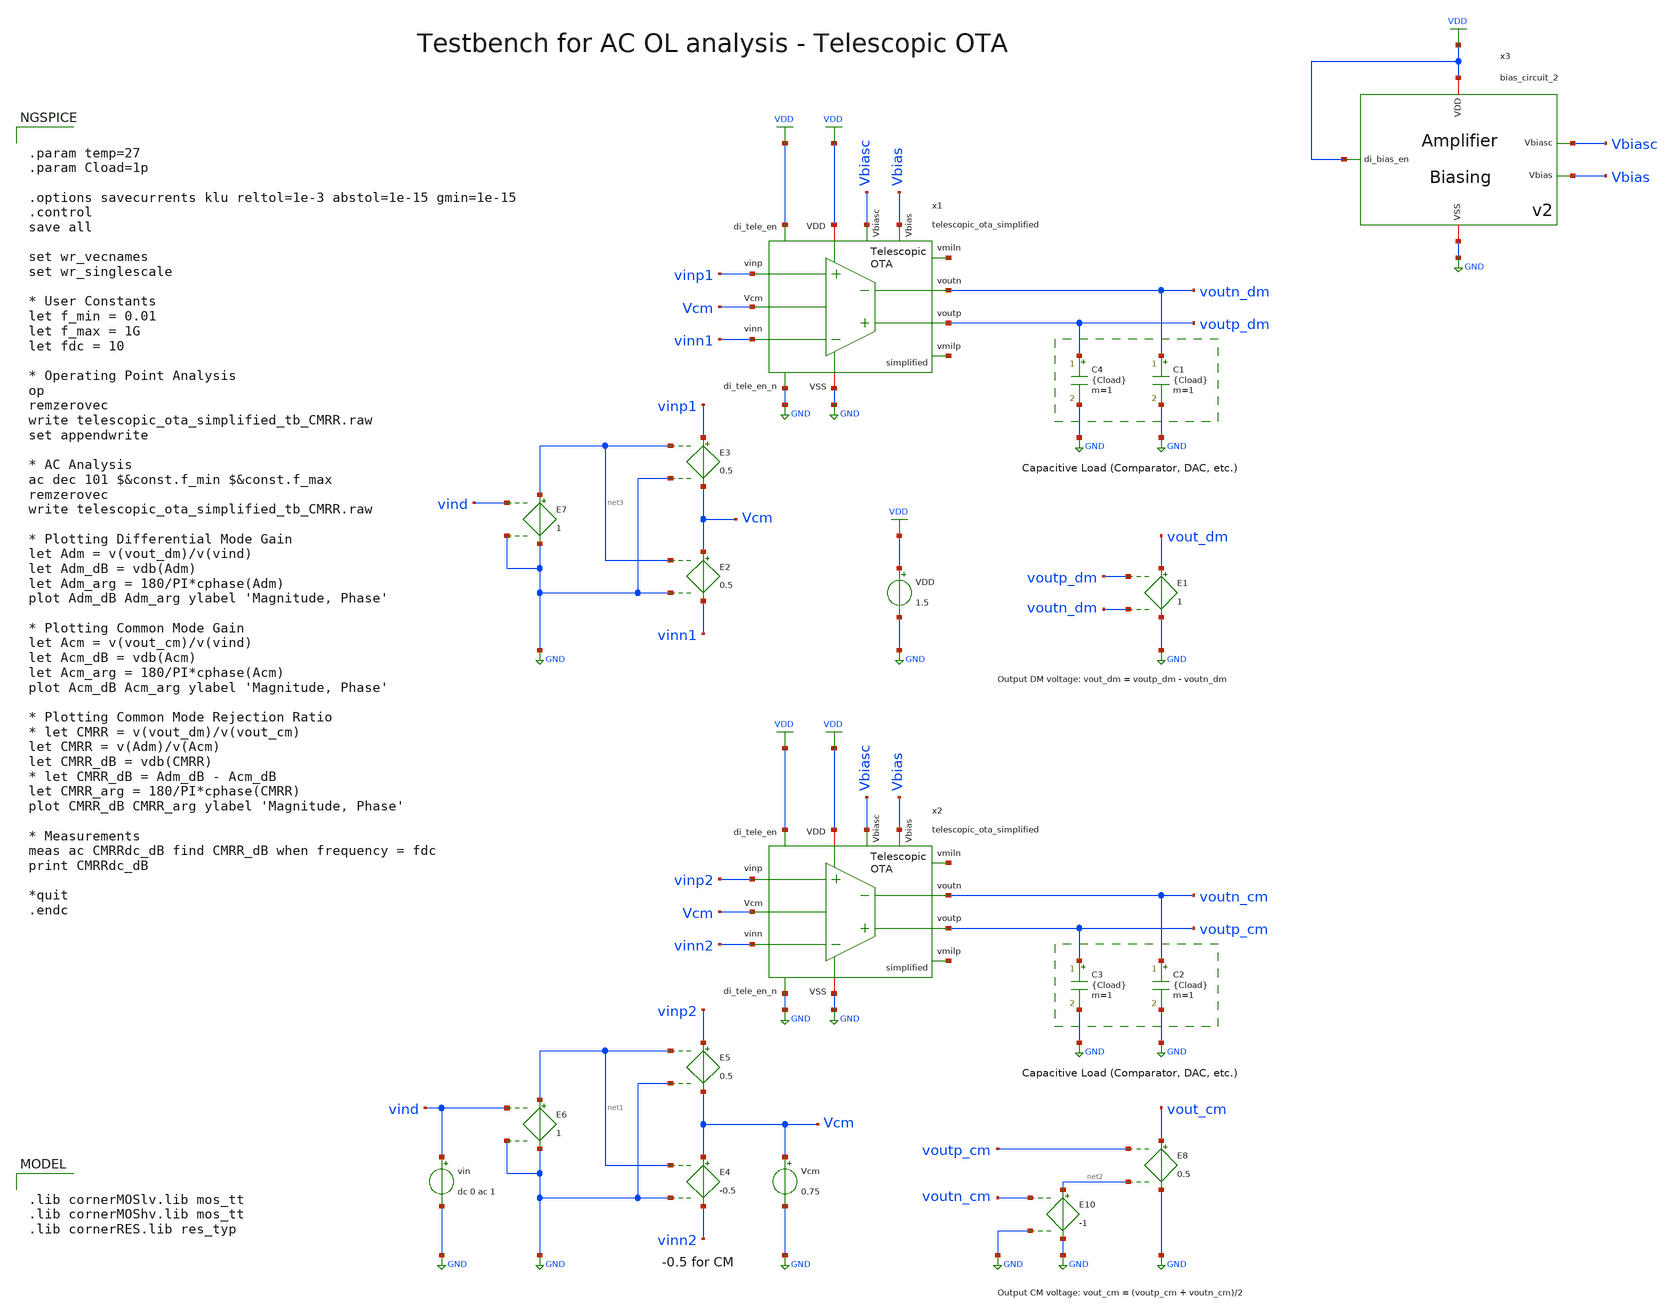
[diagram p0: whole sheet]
** sch_path: SG13G2_ATBS-ADC-main/xschem/bio_amplifier/amplifier_core/telescopic_ota/testbenches/telescopic_ota_simplified_tb_CMRR.sch
**.subckt telescopic_ota_simplified_tb_CMRR
VDD VDD GND 1.5
Vcm Vcm GND 0.75
E4 Vcm vinn2 net1 GND -0.5
E5 vinp2 Vcm net1 GND 0.5
E6 net1 GND vind GND 1
vin vind GND dc 0 ac 1
C2 voutn_cm GND {Cload} m=1
C3 voutp_cm GND {Cload} m=1
E1 vout_dm GND voutp_dm voutn_dm 1
E8 vout_cm GND voutp_cm net2 0.5
E10 net2 GND voutn_cm GND -1
E2 Vcm vinn1 net3 GND 0.5
E3 vinp1 Vcm net3 GND 0.5
E7 net3 GND vind GND 1
C1 voutn_dm GND {Cload} m=1
C4 voutp_dm GND {Cload} m=1
x1 net4 net5 voutp_dm voutn_dm VDD vinn1 vinp1 GND Vcm VDD GND Vbiasc Vbias
+ telescopic_ota_simplified
x2 net6 net7 voutp_cm voutn_cm VDD vinn2 vinp2 GND Vcm VDD GND Vbiasc Vbias
+ telescopic_ota_simplified
x3 VDD Vbiasc VDD GND Vbias bias_circuit_2
**** begin user architecture code


.param temp=27
.param Cload=1p

.options savecurrents klu reltol=1e-3 abstol=1e-15 gmin=1e-15
.control
save all

set wr_vecnames
set wr_singlescale

* User Constants
let f_min = 0.01
let f_max = 1G
let fdc = 10

* Operating Point Analysis
op
remzerovec
write telescopic_ota_simplified_tb_CMRR.raw
set appendwrite

* AC Analysis
ac dec 101 $&const.f_min $&const.f_max
remzerovec
write telescopic_ota_simplified_tb_CMRR.raw

* Plotting Differential Mode Gain
let Adm = v(vout_dm)/v(vind)
let Adm_dB = vdb(Adm)
let Adm_arg = 180/PI*cphase(Adm)
plot Adm_dB Adm_arg ylabel 'Magnitude, Phase'

* Plotting Common Mode Gain
let Acm = v(vout_cm)/v(vind)
let Acm_dB = vdb(Acm)
let Acm_arg = 180/PI*cphase(Acm)
plot Acm_dB Acm_arg ylabel 'Magnitude, Phase'

* Plotting Common Mode Rejection Ratio
* let CMRR = v(vout_dm)/v(vout_cm)
let CMRR = v(Adm)/v(Acm)
let CMRR_dB = vdb(CMRR)
* let CMRR_dB = Adm_dB - Acm_dB
let CMRR_arg = 180/PI*cphase(CMRR)
plot CMRR_dB CMRR_arg ylabel 'Magnitude, Phase'

* Measurements
meas ac CMRRdc_dB find CMRR_dB when frequency = fdc
print CMRRdc_dB

*quit
.endc



.lib cornerMOSlv.lib mos_tt
.lib cornerMOShv.lib mos_tt
.lib cornerRES.lib res_typ

**** end user architecture code
**.ends

* expanding   symbol:  bio_amplifier/amplifier_core/telescopic_ota/telescopic_ota_simplified.sym #
*+ of pins=13
** sym_path: SG13G2_ATBS-ADC-main/xschem/bio_amplifier/amplifier_core/telescopic_ota/telescopic_ota_simplified.sym
** sch_path: SG13G2_ATBS-ADC-main/xschem/bio_amplifier/amplifier_core/telescopic_ota/telescopic_ota_simplified.sch
.subckt telescopic_ota_simplified vmiln vmilp voutp voutn VDD vinn vinp VSS Vcm di_tele_en
+ di_tele_en_n Vbiasc Vbias
*.ipin vinp
*.ipin vinn
*.opin voutp
*.opin voutn
*.iopin VDD
*.iopin VSS
*.ipin Vcm
*.ipin di_tele_en
*.ipin di_tele_en_n
*.ipin vmilp
*.ipin vmiln
*.ipin Vbias
*.ipin Vbiasc
R1 net1 voutn 25.5Meg m=1
C1 net1 voutn 900f m=1
C2 voutp net1 900f m=1
R2 voutp net1 25.5Meg m=1
xM6 net3 Vgs_m56 VDD VDD sg13g2_lv_pmos_stacked_x2 W_P=1.0u L_P=20.0u NG_P=1 M_P=1
xM5 net2 Vgs_m56 VDD VDD sg13g2_lv_pmos_stacked_x2 W_P=8.0u L_P=20.0u NG_P=8 M_P=1
xM5c Vtail net10 net2 net2 sg13g2_lv_pmos_stacked_x2 W_P=8.0u L_P=20.0u NG_P=8 M_P=1
xM7 net7 net7 net6 net6 sg13g2_lv_pmos_stacked_x2 W_P=0.5u L_P=20.0u NG_P=1 M_P=1
XM1 vmiln vinp net4 net6 sg13_lv_pmos w=250.0u l=10.0u ng=250 m=1 mm_ok=1
XM1c voutn net7 vmiln vmiln sg13_lv_pmos w=15.0u l=10.0u ng=15 m=1 mm_ok=1
XM2c voutp net7 vmilp vmilp sg13_lv_pmos w=15.0u l=10.0u ng=15 m=1 mm_ok=1
XM2 vmilp vinn net5 net6 sg13_lv_pmos w=250.0u l=10.0u ng=250 m=1 mm_ok=1
xM3 voutn net1 VSS VSS sg13g2_lv_nmos_stacked_x4 W_N=1.5u L_N=40.0u NG_N=1 M_N=1
xM4 voutp net1 VSS VSS sg13g2_lv_nmos_stacked_x4 W_N=1.5u L_N=40.0u NG_N=1 M_N=1
Vmeas net9 net4 0
.save i(vmeas)
Vmeas1 net9 net5 0
.save i(vmeas1)
Vmeas2 net9 net6 0
.save i(vmeas2)
xM6c net8 net10 net3 net3 sg13g2_lv_pmos_stacked_x2 W_P=1.0u L_P=20.0u NG_P=1 M_P=1
XMpd4 Vcm di_tele_en_n net10 VDD sg13_hv_pmos w=1.0u l=0.5u ng=1 m=1 mm_ok=1
XMdec1 VDD Vgs_m56 VDD VDD sg13_lv_pmos w=10.0u l=40.0u ng=10 m=1 mm_ok=1
XMpd3 net10 di_tele_en VDD VDD sg13_hv_pmos w=1.0u l=0.5u ng=1 m=1 mm_ok=1
XMpd2 net8 di_tele_en_n Vgs_m56 VDD sg13_hv_pmos w=1.0u l=0.5u ng=1 m=1 mm_ok=1
XMpd1 Vgs_m56 di_tele_en VDD VDD sg13_hv_pmos w=1.0u l=0.5u ng=1 m=1 mm_ok=1
XMdec3 VDD net10 VDD VDD sg13_lv_pmos w=10.0u l=40.0u ng=10 m=1 mm_ok=1
Vmeas3 net8 net12 0
.save i(vmeas3)
Vmeas4 net7 net14 0
.save i(vmeas4)
xM8c net12 Vbiasc VSS net11 sg13g2_lv_nmos_stacked_x2 W_N=20.0u L_N=20.0u NG_N=20 M_N=1
xM8 net11 Vbias VSS VSS sg13g2_lv_nmos_stacked_x2 W_N=20.0u L_N=20.0u NG_N=20 M_N=1
xM9c net14 Vbiasc VSS net13 sg13g2_lv_nmos_stacked_x2 W_N=10.0u L_N=20.0u NG_N=10 M_N=1
xM9 net13 Vbias VSS VSS sg13g2_lv_nmos_stacked_x2 W_N=10.0u L_N=20.0u NG_N=10 M_N=1
Vmeas5 Vtail net9 0
.save i(vmeas5)
.ends


* expanding   symbol:  bio_amplifier/amplifier_core/bias_circuit/bias_circuit_2/bias_circuit_2.sym #
*+ of pins=5
** sym_path: SG13G2_ATBS-ADC-main/xschem/bio_amplifier/amplifier_core/bias_circuit/bias_circuit_2/bias_circuit_2.sym
** sch_path: SG13G2_ATBS-ADC-main/xschem/bio_amplifier/amplifier_core/bias_circuit/bias_circuit_2/bias_circuit_2.sch
.subckt bias_circuit_2 di_bias_en Vbiasc VDD VSS Vbias
*.iopin VDD
*.iopin VSS
*.opin Vbias
*.ipin di_bias_en
*.opin Vbiasc
R1 net3 VSS 3.72Meg m=1
XMDEC1 net1 Vbias net1 net1 sg13_lv_nmos w=100.0u l=40.0u ng=100 m=1 mm_ok=1
VIref net4 net8 0
.save i(viref)
VIout net9 Vbiasc 0
.save i(viout)
x1 VDD di_bias_en bias_en_n VSS inverter_lv W_P=1.0u L_P=0.13u W_N=1.0u L_N=0.13u
xMSU2 Vsu net6 VSS VSS sg13g2_lv_nmos_stacked_x4 W_N=1.0u L_N=40.0u NG_N=1 M_N=1
xMSU1 net5 Vsu VSS net6 sg13g2_lv_nmos_stacked_x4 W_N=1.0u L_N=40.0u NG_N=1 M_N=1
Vmeas1 net4 net5 0
.save i(vmeas1)
Vmeas2 Vbias net6 0
.save i(vmeas2)
XMPD1 Vgs_m34 di_bias_en net2 net2 sg13_lv_pmos w=1.0u l=0.13u ng=1 m=1 mm_ok=1
XMPD2 net4 bias_en_n Vgs_m34 net2 sg13_lv_pmos w=1.0u l=0.13u ng=1 m=1 mm_ok=1
XMPD3 Vbias bias_en_n VSS VSS sg13_lv_nmos w=1.0u l=0.13u ng=1 m=1 mm_ok=1
VIref5 net1 VSS 0
.save i(viref5)
VIdd VDD net2 0
.save i(vidd)
CSU1 net10 Vsu 35f m=1
xM1 net7 Vbias VSS net3 sg13g2_lv_nmos_stacked_x2 W_N=20.0u L_N=20.0u NG_N=20 M_N=1
xM1c net8 Vbiasc VSS net7 sg13g2_lv_nmos_stacked_x2 W_N=5.0u L_N=20.0u NG_N=5 M_N=1
xM2 Vbias Vbias VSS VSS sg13g2_lv_nmos_stacked_x2 W_N=5.0u L_N=20.0u NG_N=5 M_N=1
xM2c Vbiasc Vbiasc VSS Vbias sg13g2_lv_nmos_stacked_x2 W_N=5.0u L_N=20.0u NG_N=5 M_N=1
XMDEC2 net2 Vgs_m34 net2 net2 sg13_lv_pmos w=25.0u l=40.0u ng=25 m=1 mm_ok=1
xM3 net4 Vgs_m34 net2 net2 sg13g2_lv_pmos_stacked_x4 W_P=20.0u L_P=40.0u NG_P=20 M_P=1
xM4 net9 Vgs_m34 net2 net2 sg13g2_lv_pmos_stacked_x4 W_P=20.0u L_P=40.0u NG_P=20 M_P=1
XMPD6 Vsu di_bias_en net10 net10 sg13_lv_pmos w=1.0u l=0.13u ng=1 m=1 mm_ok=1
XMPD4 Vbiasc bias_en_n VSS VSS sg13_lv_nmos w=1.0u l=0.13u ng=1 m=1 mm_ok=1
XMPD7 Vsu bias_en_n VSS VSS sg13_lv_nmos w=1.0u l=0.13u ng=1 m=1 mm_ok=1
XMPD5 net10 bias_en_n net2 net2 sg13_lv_pmos w=1.0u l=0.13u ng=1 m=1 mm_ok=1
.ends


* expanding   symbol:  stacked_transistors/sg13g2_lv_pmos_stacked/sg13g2_lv_pmos_stacked_x2.sym # of
*+ pins=4
** sym_path: SG13G2_ATBS-ADC-main/xschem/stacked_transistors/sg13g2_lv_pmos_stacked/sg13g2_lv_pmos_stacked_x2.sym
** sch_path: SG13G2_ATBS-ADC-main/xschem/stacked_transistors/sg13g2_lv_pmos_stacked/sg13g2_lv_pmos_stacked_x2.sch
.subckt sg13g2_lv_pmos_stacked_x2 D G B S  W_P=1.0u L_P=0.45u NG_P=1 M_P=1
*.iopin D
*.iopin S
*.iopin G
*.iopin B
XM1 net1 G S B sg13_lv_pmos w=W_P l=L_P/2 ng=NG_P m=M_P mm_ok=1
XM2 D G net1 B sg13_lv_pmos w=W_P l=L_P/2 ng=NG_P m=M_P mm_ok=1
.ends


* expanding   symbol:  stacked_transistors/sg13g2_lv_nmos_stacked/sg13g2_lv_nmos_stacked_x4.sym # of
*+ pins=4
** sym_path: SG13G2_ATBS-ADC-main/xschem/stacked_transistors/sg13g2_lv_nmos_stacked/sg13g2_lv_nmos_stacked_x4.sym
** sch_path: SG13G2_ATBS-ADC-main/xschem/stacked_transistors/sg13g2_lv_nmos_stacked/sg13g2_lv_nmos_stacked_x4.sch
.subckt sg13g2_lv_nmos_stacked_x4 D G B S  W_N=1.0u L_N=0.45u NG_N=1 M_N=1
*.iopin D
*.iopin S
*.iopin G
*.iopin B
XM1 net1 G S B sg13_lv_nmos w=W_N l=L_N/4 ng=NG_N m=M_N mm_ok=1
XM2 net3 G net1 B sg13_lv_nmos w=W_N l=L_N/4 ng=NG_N m=M_N mm_ok=1
XM3 net2 G net3 B sg13_lv_nmos w=W_N l=L_N/4 ng=NG_N m=M_N mm_ok=1
XM4 D G net2 B sg13_lv_nmos w=W_N l=L_N/4 ng=NG_N m=M_N mm_ok=1
.ends


* expanding   symbol:  stacked_transistors/sg13g2_lv_nmos_stacked/sg13g2_lv_nmos_stacked_x2.sym # of
*+ pins=4
** sym_path: SG13G2_ATBS-ADC-main/xschem/stacked_transistors/sg13g2_lv_nmos_stacked/sg13g2_lv_nmos_stacked_x2.sym
** sch_path: SG13G2_ATBS-ADC-main/xschem/stacked_transistors/sg13g2_lv_nmos_stacked/sg13g2_lv_nmos_stacked_x2.sch
.subckt sg13g2_lv_nmos_stacked_x2 D G B S  W_N=1.0u L_N=0.45u NG_N=1 M_N=1
*.iopin D
*.iopin S
*.iopin G
*.iopin B
XM1 net1 G S B sg13_lv_nmos w=W_N l=L_N/2 ng=NG_N m=M_N mm_ok=1
XM2 D G net1 B sg13_lv_nmos w=W_N l=L_N/2 ng=NG_N m=M_N mm_ok=1
.ends


* expanding   symbol:  inverter/inverter_lv.sym # of pins=4
** sym_path: SG13G2_ATBS-ADC-main/xschem/inverter/inverter_lv.sym
** sch_path: SG13G2_ATBS-ADC-main/xschem/inverter/inverter_lv.sch
.subckt inverter_lv VDD vin vout VSS  W_P=3.0u L_P=0.13u W_N=1.0u L_N=0.13u
*.ipin vin
*.iopin VDD
*.iopin VSS
*.opin vout
XM1 vout vin VDD VDD sg13_lv_pmos w=W_P l=L_P ng=1 m=1 mm_ok=1
XM2 vout vin VSS VSS sg13_lv_nmos w=W_N l=L_N ng=1 m=1 mm_ok=1
.ends


* expanding   symbol:  stacked_transistors/sg13g2_lv_pmos_stacked/sg13g2_lv_pmos_stacked_x4.sym # of
*+ pins=4
** sym_path: SG13G2_ATBS-ADC-main/xschem/stacked_transistors/sg13g2_lv_pmos_stacked/sg13g2_lv_pmos_stacked_x4.sym
** sch_path: SG13G2_ATBS-ADC-main/xschem/stacked_transistors/sg13g2_lv_pmos_stacked/sg13g2_lv_pmos_stacked_x4.sch
.subckt sg13g2_lv_pmos_stacked_x4 D G B S  W_P=1.0u L_P=0.45u NG_P=1 M_P=1
*.iopin D
*.iopin S
*.iopin G
*.iopin B
XM1 net1 G S B sg13_lv_pmos w=W_P l=L_P/4 ng=NG_P m=M_P mm_ok=1
XM2 net3 G net1 B sg13_lv_pmos w=W_P l=L_P/4 ng=NG_P m=M_P mm_ok=1
XM3 net2 G net3 B sg13_lv_pmos w=W_P l=L_P/4 ng=NG_P m=M_P mm_ok=1
XM4 D G net2 B sg13_lv_pmos w=W_P l=L_P/4 ng=NG_P m=M_P mm_ok=1
.ends

.GLOBAL GND
.GLOBAL VDD
.end
